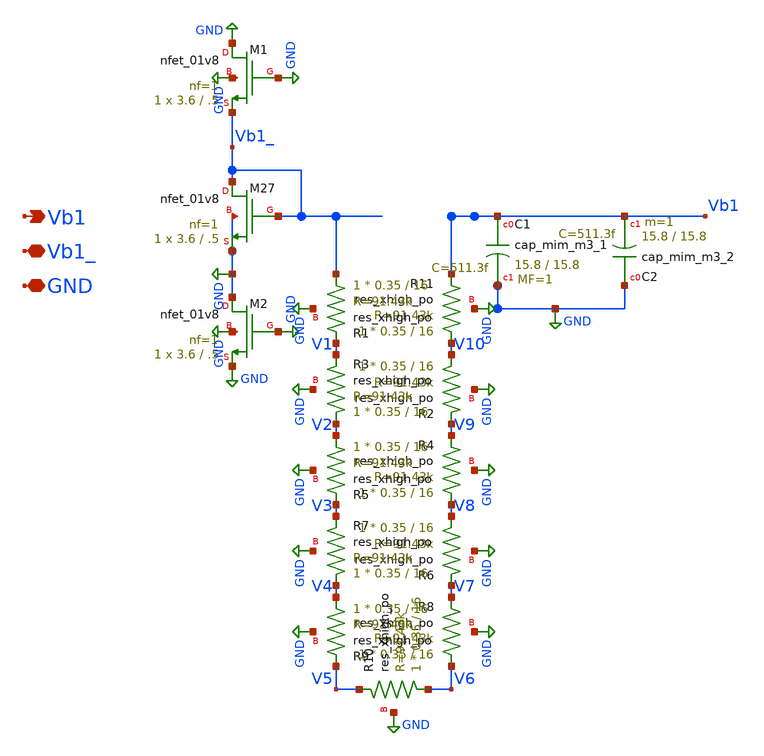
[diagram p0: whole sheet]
** sch_path: xschem/mirror_1.sch
**.subckt mirror_1 GND Vb1_ Vb1
*.iopin GND
*.iopin Vb1_
*.opin Vb1
XM27 Vb1_ Vb1_ GND GND sky130_fd_pr__nfet_01v8 L=.5 W=3.6 nf=1 ad='int((nf+1)/2) * W/nf * 0.29' as='int((nf+2)/2) * W/nf * 0.29'
+ pd='2*int((nf+1)/2) * (W/nf + 0.29)' ps='2*int((nf+2)/2) * (W/nf + 0.29)' nrd='0.29 / W' nrs='0.29 / W'
+ sa=0 sb=0 sd=0 mult=1 m=1
XC1 Vb1 GND sky130_fd_pr__cap_mim_m3_1 W=15.8 L=15.8 MF=1 m=1
XC2 GND Vb1 sky130_fd_pr__cap_mim_m3_2 W=15.8 L=15.8 MF=1 m=1
XR11 V10 Vb1 GND sky130_fd_pr__res_xhigh_po W=0.35 L=16 mult=1 m=1
XR1 Vb1_ V1 GND sky130_fd_pr__res_xhigh_po W=0.35 L=16 mult=1 m=1
XR2 V10 V9 GND sky130_fd_pr__res_xhigh_po W=0.35 L=16 mult=1 m=1
XR3 V2 V1 GND sky130_fd_pr__res_xhigh_po W=0.35 L=16 mult=1 m=1
XR4 V8 V9 GND sky130_fd_pr__res_xhigh_po W=0.35 L=16 mult=1 m=1
XR5 V2 V3 GND sky130_fd_pr__res_xhigh_po W=0.35 L=16 mult=1 m=1
XR6 V8 V7 GND sky130_fd_pr__res_xhigh_po W=0.35 L=16 mult=1 m=1
XR7 V4 V3 GND sky130_fd_pr__res_xhigh_po W=0.35 L=16 mult=1 m=1
XR8 V6 V7 GND sky130_fd_pr__res_xhigh_po W=0.35 L=16 mult=1 m=1
XR9 V4 V5 GND sky130_fd_pr__res_xhigh_po W=0.35 L=16 mult=1 m=1
XR10 V6 V5 GND sky130_fd_pr__res_xhigh_po W=0.35 L=16 mult=1 m=1
XM1 GND GND Vb1_ GND sky130_fd_pr__nfet_01v8 L=.5 W=3.6 nf=1 ad='int((nf+1)/2) * W/nf * 0.29' as='int((nf+2)/2) * W/nf * 0.29'
+ pd='2*int((nf+1)/2) * (W/nf + 0.29)' ps='2*int((nf+2)/2) * (W/nf + 0.29)' nrd='0.29 / W' nrs='0.29 / W'
+ sa=0 sb=0 sd=0 mult=1 m=1
XM2 GND GND GND GND sky130_fd_pr__nfet_01v8 L=.5 W=3.6 nf=1 ad='int((nf+1)/2) * W/nf * 0.29' as='int((nf+2)/2) * W/nf * 0.29'
+ pd='2*int((nf+1)/2) * (W/nf + 0.29)' ps='2*int((nf+2)/2) * (W/nf + 0.29)' nrd='0.29 / W' nrs='0.29 / W'
+ sa=0 sb=0 sd=0 mult=1 m=1
**.ends
.GLOBAL GND
.end
